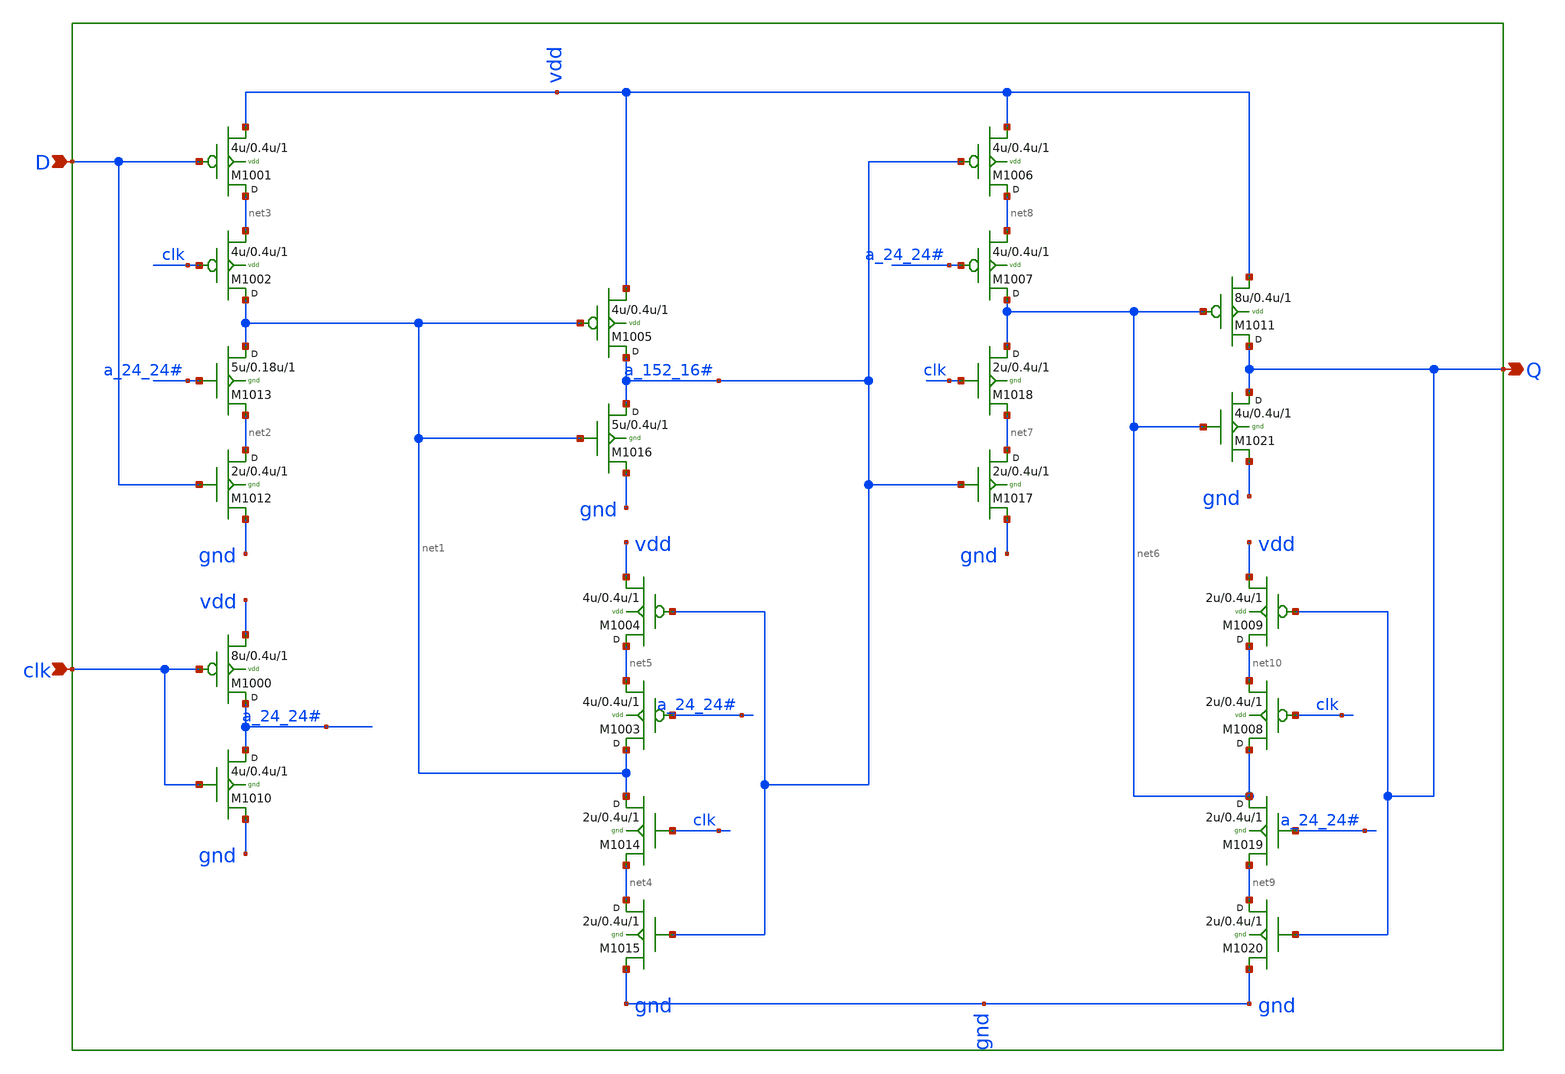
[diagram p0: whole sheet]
** sch_path: sram_2_64_scn4m_lcc/dff.sch
**.subckt dff D clk Q
*.ipin D
*.ipin clk
*.opin Q
M1013 net1 a_24_24# net2 gnd n w=5u l=0.18u m=1
M1012 net2 D gnd gnd n w=2u l=0.4u m=1
M1001 net3 D vdd vdd p w=4u l=0.4u m=1
M1002 net1 clk net3 vdd p w=4u l=0.4u m=1
M1000 a_24_24# clk vdd vdd p w=8u l=0.4u m=1
M1010 a_24_24# clk gnd gnd n w=4u l=0.4u m=1
M1005 a_152_16# net1 vdd vdd p w=4u l=0.4u m=1
M1016 a_152_16# net1 gnd gnd n w=5u l=0.4u m=1
M1004 net5 a_152_16# vdd vdd p w=4u l=0.4u m=1
M1003 net1 a_24_24# net5 vdd p w=4u l=0.4u m=1
M1014 net1 clk net4 gnd n w=2u l=0.4u m=1
M1015 net4 a_152_16# gnd gnd n w=2u l=0.4u m=1
M1006 net8 a_152_16# vdd vdd p w=4u l=0.4u m=1
M1007 net6 a_24_24# net8 vdd p w=4u l=0.4u m=1
M1018 net6 clk net7 gnd n w=2u l=0.4u m=1
M1017 net7 a_152_16# gnd gnd n w=2u l=0.4u m=1
M1021 Q net6 gnd gnd n w=4u l=0.4u m=1
M1011 Q net6 vdd vdd p w=8u l=0.4u m=1
M1020 net9 Q gnd gnd n w=2u l=0.4u m=1
M1019 net6 a_24_24# net9 gnd n w=2u l=0.4u m=1
M1009 net10 Q vdd vdd p w=2u l=0.4u m=1
M1008 net6 clk net10 vdd p w=2u l=0.4u m=1
**.ends
.end
